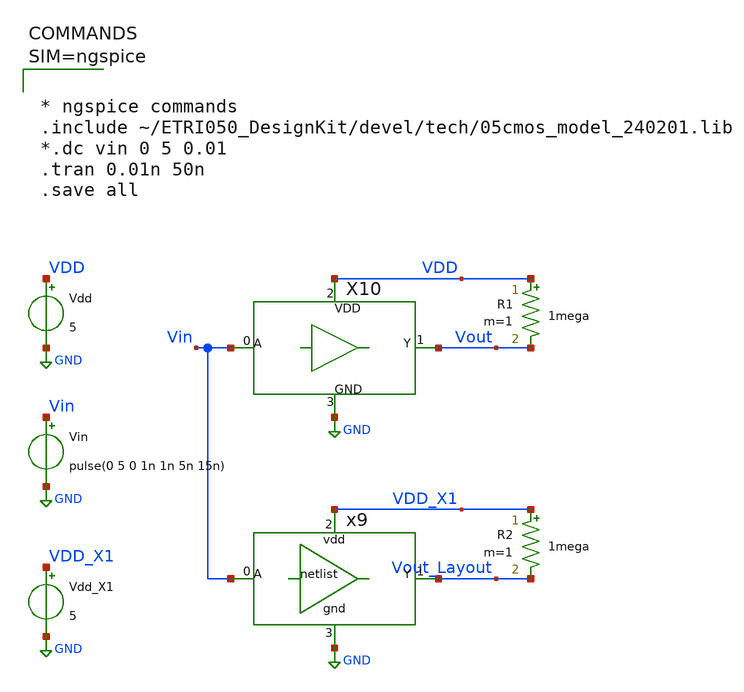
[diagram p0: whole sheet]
** sch_path: Tutorials/1-3_Inverter_Netgen/buffer_TB_tran.sch
**.subckt buffer_TB_tran
Vdd VDD GND 5
R1 VDD Vout 1mega m=1
R2 VDD_X1 Vout_Layout 1mega m=1
Vin Vin GND pulse(0 5 0 1n 1n 5n 15n)
Vdd_X1 VDD_X1 GND 5
x9 Vin Vout_Layout VDD_X1 GND buffer_x1
X10 Vin Vout VDD GND buffer
**** begin user architecture code



* ngspice commands
.include ~/ETRI050_DesignKit/devel/tech/05cmos_model_240201.lib
*.dc vin 0 5 0.01
.tran 0.01n 50n
.save all



**** end user architecture code
**.ends
.GLOBAL GND
.end
